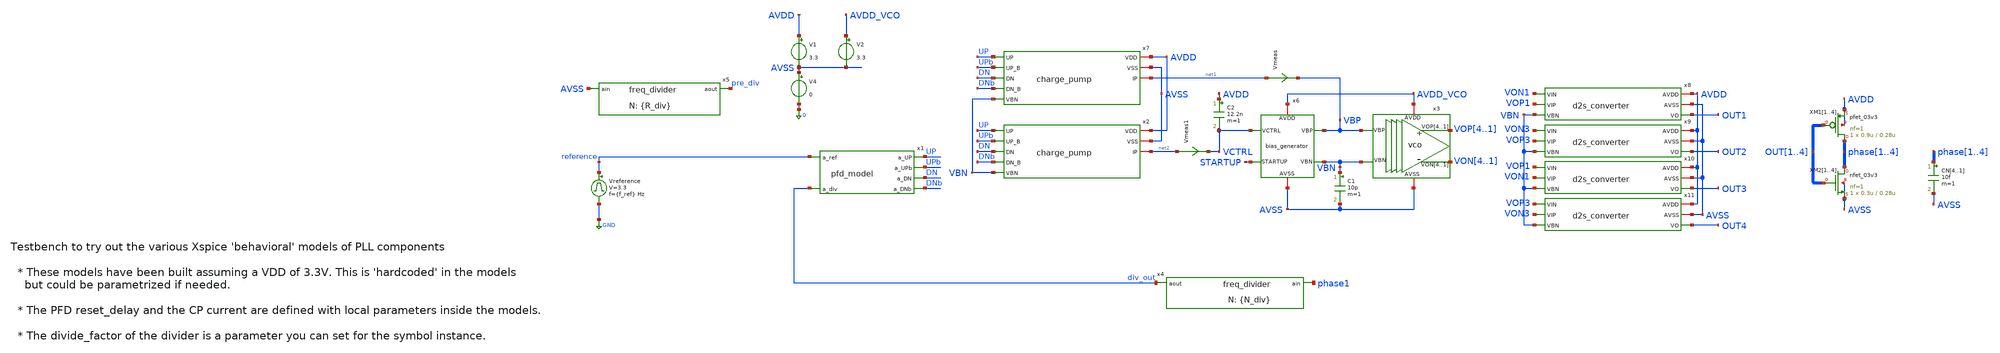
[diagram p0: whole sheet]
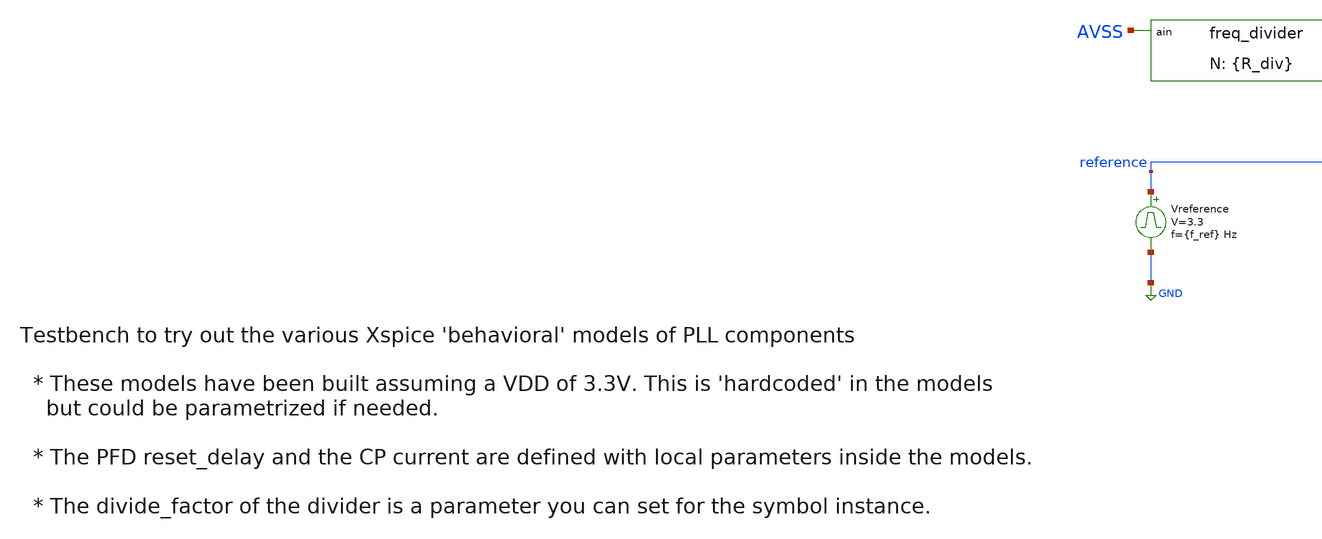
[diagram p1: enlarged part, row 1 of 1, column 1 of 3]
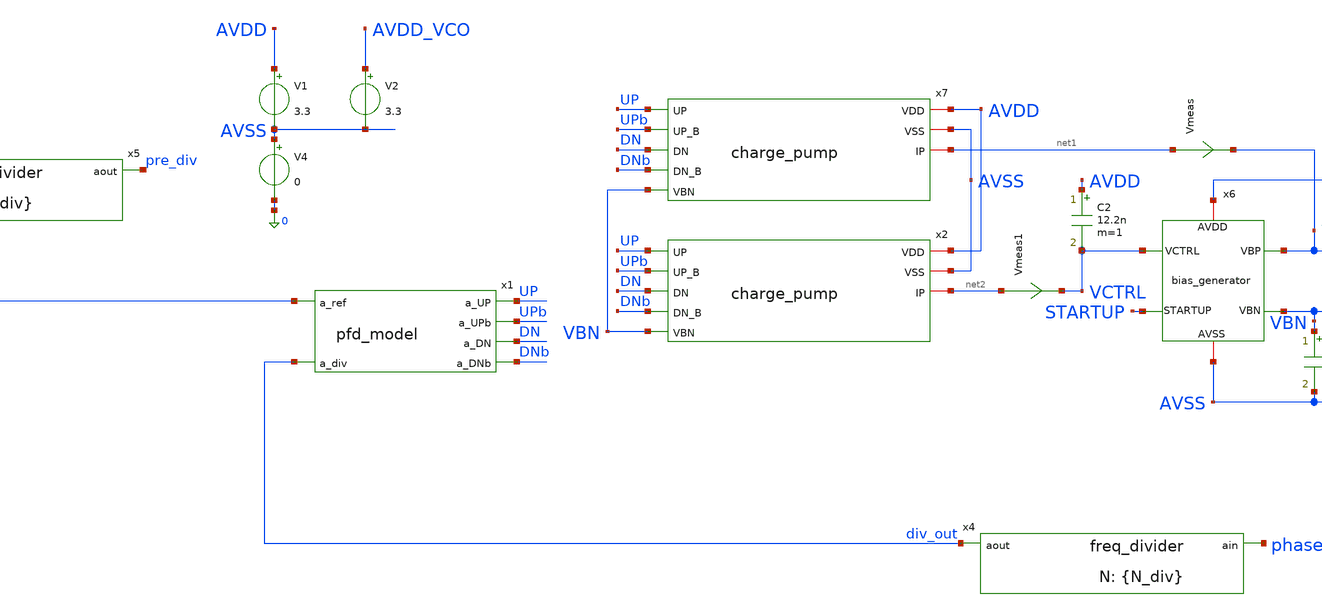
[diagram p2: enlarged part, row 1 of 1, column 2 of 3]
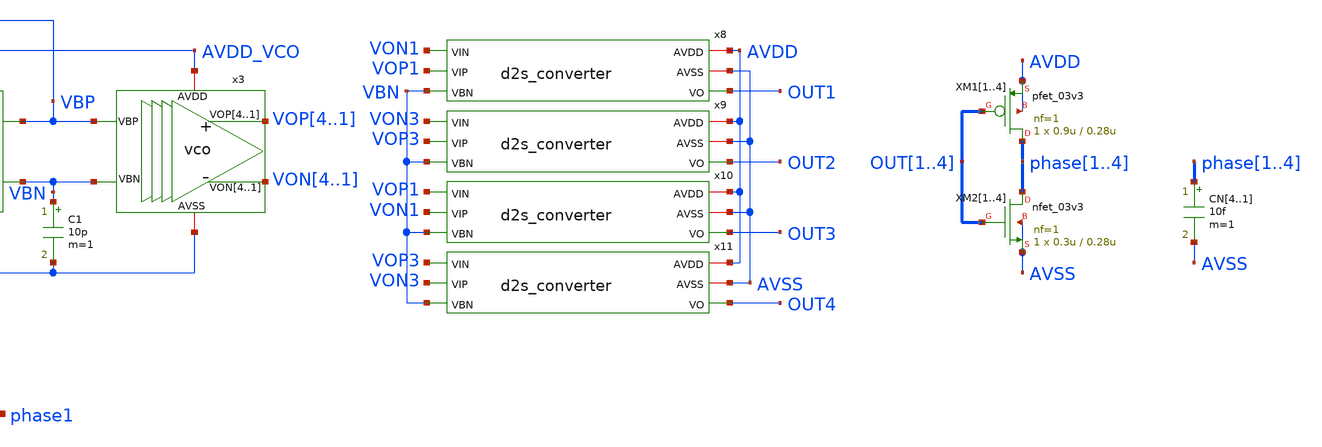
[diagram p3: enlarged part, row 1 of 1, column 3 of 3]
** sch_path: designs/libs/tb_pll/tb_PLL_CP_VCO_model_v2.sch
**.subckt tb_PLL_CP_VCO_model_v2
Vreference reference GND pulse 0 3.3 '0.495/ {f_ref} ' '0.01/{f_ref} ' '0.01/{f_ref} ' '0.49/{f_ref} '
+ '1/{f_ref} '
x1 reference UP UPb DN div_out DNb pfd_model
x4 div_out phase1 freq_divider divide_factor={N_div}
x5 pre_div AVSS freq_divider divide_factor={R_div}
x3 VOP4 VOP3 VOP2 VOP1 VON4 VON3 VON2 VON1 AVDD_VCO AVSS VBP VBN vco
x6 VCTRL AVDD_VCO STARTUP AVSS VBP VBN bias_generator
C1 VBN AVSS 10p m=1
C2 AVDD VCTRL 12.2n m=1
x8 AVDD AVSS VON1 VOP1 VBN OUT1 d2s_converter
XM11 phase1 OUT1 AVDD AVDD pfet_03v3 L=0.28u W=0.9u nf=1 ad='int((nf+1)/2) * W/nf * 0.18u' as='int((nf+2)/2) * W/nf * 0.18u'
+ pd='2*int((nf+1)/2) * (W/nf + 0.18u)' ps='2*int((nf+2)/2) * (W/nf + 0.18u)' nrd='0.18u / W' nrs='0.18u / W'
+ sa=0 sb=0 sd=0 m=1
XM12 phase2 OUT2 AVDD AVDD pfet_03v3 L=0.28u W=0.9u nf=1 ad='int((nf+1)/2) * W/nf * 0.18u' as='int((nf+2)/2) * W/nf * 0.18u'
+ pd='2*int((nf+1)/2) * (W/nf + 0.18u)' ps='2*int((nf+2)/2) * (W/nf + 0.18u)' nrd='0.18u / W' nrs='0.18u / W'
+ sa=0 sb=0 sd=0 m=1
XM13 phase3 OUT3 AVDD AVDD pfet_03v3 L=0.28u W=0.9u nf=1 ad='int((nf+1)/2) * W/nf * 0.18u' as='int((nf+2)/2) * W/nf * 0.18u'
+ pd='2*int((nf+1)/2) * (W/nf + 0.18u)' ps='2*int((nf+2)/2) * (W/nf + 0.18u)' nrd='0.18u / W' nrs='0.18u / W'
+ sa=0 sb=0 sd=0 m=1
XM14 phase4 OUT4 AVDD AVDD pfet_03v3 L=0.28u W=0.9u nf=1 ad='int((nf+1)/2) * W/nf * 0.18u' as='int((nf+2)/2) * W/nf * 0.18u'
+ pd='2*int((nf+1)/2) * (W/nf + 0.18u)' ps='2*int((nf+2)/2) * (W/nf + 0.18u)' nrd='0.18u / W' nrs='0.18u / W'
+ sa=0 sb=0 sd=0 m=1
XM21 phase1 OUT1 AVSS AVSS nfet_03v3 L=0.28u W=0.3u nf=1 ad='int((nf+1)/2) * W/nf * 0.18u' as='int((nf+2)/2) * W/nf * 0.18u'
+ pd='2*int((nf+1)/2) * (W/nf + 0.18u)' ps='2*int((nf+2)/2) * (W/nf + 0.18u)' nrd='0.18u / W' nrs='0.18u / W'
+ sa=0 sb=0 sd=0 m=1
XM22 phase2 OUT2 AVSS AVSS nfet_03v3 L=0.28u W=0.3u nf=1 ad='int((nf+1)/2) * W/nf * 0.18u' as='int((nf+2)/2) * W/nf * 0.18u'
+ pd='2*int((nf+1)/2) * (W/nf + 0.18u)' ps='2*int((nf+2)/2) * (W/nf + 0.18u)' nrd='0.18u / W' nrs='0.18u / W'
+ sa=0 sb=0 sd=0 m=1
XM23 phase3 OUT3 AVSS AVSS nfet_03v3 L=0.28u W=0.3u nf=1 ad='int((nf+1)/2) * W/nf * 0.18u' as='int((nf+2)/2) * W/nf * 0.18u'
+ pd='2*int((nf+1)/2) * (W/nf + 0.18u)' ps='2*int((nf+2)/2) * (W/nf + 0.18u)' nrd='0.18u / W' nrs='0.18u / W'
+ sa=0 sb=0 sd=0 m=1
XM24 phase4 OUT4 AVSS AVSS nfet_03v3 L=0.28u W=0.3u nf=1 ad='int((nf+1)/2) * W/nf * 0.18u' as='int((nf+2)/2) * W/nf * 0.18u'
+ pd='2*int((nf+1)/2) * (W/nf + 0.18u)' ps='2*int((nf+2)/2) * (W/nf + 0.18u)' nrd='0.18u / W' nrs='0.18u / W'
+ sa=0 sb=0 sd=0 m=1
x9 AVDD AVSS VON3 VOP3 VBN OUT2 d2s_converter
x10 AVDD AVSS VOP1 VON1 VBN OUT3 d2s_converter
x11 AVDD AVSS VOP3 VON3 VBN OUT4 d2s_converter
V1 AVDD AVSS 3.3
V4 AVSS 0 0
V2 AVDD_VCO AVSS 3.3
CN4 phase1 AVSS 10f m=1
CN3 phase2 AVSS 10f m=1
CN2 phase3 AVSS 10f m=1
CN1 phase4 AVSS 10f m=1
Vmeas net1 VBP 0
.save i(vmeas)
Vmeas1 net2 VCTRL 0
.save i(vmeas1)
x2 AVDD AVSS UP UPb DN DNb VBN net2 charge_pump
x7 AVDD AVSS UP UPb DN DNb VBN net1 charge_pump
**** begin user architecture code


.param f_ref=10MEG R_div=2 N_div=20
.ic v(vop1)=3.3 v(von1)=0 v(startup)=0 v(VCTRL)=1 v(vbp)=1

.param d1=0 d2=3.3 d3=3.3 d4=0
.param d1b=3.3 d2b=0 d3b=0 d4b=3.3

VS1 S1 0 d1
VS2 S2 0 d2
VS3 S3 0 d3
VS4 S4 0 d4

VS1b S1b 0 d1b
VS2b S2b 0 d2b
VS3b S3b 0 d3b
VS4b S4b 0 d4b

.control

save all

OP
show all

tran 1n 10u

remzerovec

write tb_PLL_CP_VCO_model_v2.raw
.endc



.include $::180MCU_MODELS/design.ngspice
.lib $::180MCU_MODELS/sm141064.ngspice typical
*.lib $::180MCU_MODELS/sm141064.ngspice SS
*.lib $::180MCU_MODELS/sm141064.ngspice FF
*.lib $::180MCU_MODELS/sm141064.ngspice SF
*.lib $::180MCU_MODELS/sm141064.ngspice FS

**** end user architecture code
**.ends

* expanding   symbol:  libs/model_pll/pfd_model.sym # of pins=6
** sym_path: designs/libs/model_pll/pfd_model.sym
** sch_path: designs/libs/model_pll/pfd_model.sch
.subckt pfd_model a_ref a_UP a_UPb a_DN a_div a_DNb
*.ipin a_ref
*.ipin a_div
*.opin a_UP
*.opin a_UPb
*.opin a_DN
*.opin a_DNb
* noconn a_ref
* noconn a_div
* noconn a_UP
* noconn a_UPb
* noconn a_DN
* noconn a_DNb
**** begin user architecture code


* PFD Model using digital Xspice components

* pfd_delay local parameter sets the duration of the overlap (dead-band elimination)
* Reduced from 10ns to 200ps to prevent massive Vctrl ripple
*.param pfd_delay = 200p
.param pfd_delay = 1.5n

** Digital 1 and 0 to drive Flip-Flops
aone 0 d_d1 d_inv
azero d_d1 d_d0 d_inv
.model d_inv d_inverter()

** Flip Flops
ad1 d_d1 d_R d_d0 d_rset d_U d_U_ flop1
ad2 d_d1 d_V d_d0 d_rset d_D d_D_ flop1
.model flop1 d_dff(clk_delay = 1.0e-10 set_delay = 1.0e-10  reset_delay = {pfd_delay} ic = 2 rise_delay
+ = 1.0e-10  fall_delay = 1e-10)

* AND Gate
aa1 [d_U d_D] d_rset and1
.model and1 d_and(rise_delay = 1e-10 fall_delay = 1e-10   input_load = 0.5e-12)

* WINDOW FIX: Widened thresholds to catch fast analog edges safely
aADC [ a_ref a_div ] [ d_R d_V ] adc_buff
.model adc_buff adc_bridge(in_low = 1.2 in_high = 2.1 rise_delay = 10p fall_delay = 10p)

* DAC FIX: Explicitly defined analog rise/fall times to prevent solver crashes
aDAC [ d_U d_U_ d_D d_D_ d_rset d_R d_V d_d1 d_d0 ] [ a_UP a_UPb a_DN a_DNb a_rset a_R a_V a_d1
+ a_d0] dac_buff
.model dac_buff dac_bridge(out_low = 0 out_high = 3.3 t_rise = 500p t_fall = 500p)


**** end user architecture code
.ends


* expanding   symbol:  libs/model_pll/freq_divider.sym # of pins=2
** sym_path: libs/model_pll/freq_divider.sym
** sch_path: libs/model_pll/freq_divider.sch
.subckt freq_divider aout ain  divide_factor=20
*.ipin ain
*.opin aout
* noconn ain
* noconn aout
**** begin user architecture code


* Behavioral Frequency Divider with robust Mixed-Signal Bridges

* Top-level parameter (Defaults to 10 if not passed by symbol)
.param divide_factor = 10

* MATH FIX: Guarantees at least 1 high cycle, targets 50% duty cycle
.param high_cycles = {max(1, floor(divide_factor/2))}

* Xspice digital frequency divider
adiv din dout divider
.model divider d_fdiv(div_factor = {divide_factor}  high_cycles = {high_cycles}  i_count = 0  rise_delay
+ = 10p fall_delay = 10p )

* WINDOW FIX: Widened analog-to-digital thresholds to catch fast sine waves
aADC [ ain ] [ din ] adc_buff
.model adc_buff adc_bridge(in_low = 1.2 in_high = 2.1 rise_delay = 10p fall_delay = 10p)

* Digital-to-analog bridge
aDAC [ dout ] [ aout ] dac_buff
.model dac_buff dac_bridge(out_low = 0 out_high = 3.3 t_rise = 10p t_fall = 10p)


**** end user architecture code
.ends


* expanding   symbol:  libs/core_analog/vco/vco.sym # of pins=6
** sym_path: designs/libs/core_analog/vco/vco.sym
** sch_path: designs/libs/core_analog/vco/vco.sch
.subckt vco VOP4 VOP3 VOP2 VOP1 VON4 VON3 VON2 VON1 AVDD AVSS VBP VBN
*.opin VOP1,VOP2,VOP3,VOP4
*.opin VON1,VON2,VON3,VON4
*.ipin VBP
*.ipin VBN
*.iopin AVDD
*.iopin AVSS
x1 VOP1 AVDD VOP4 VON4 VON1 AVSS VBP VBN delay_stage
x2 VOP2 AVDD VON1 VOP1 VON2 AVSS VBP VBN delay_stage
x3 VOP3 AVDD VON2 VOP2 VON3 AVSS VBP VBN delay_stage
x4 VOP4 AVDD VON3 VOP3 VON4 AVSS VBP VBN delay_stage
.ends


* expanding   symbol:  libs/core_analog/bias_generator/bias_generator.sym # of pins=6
** sym_path: designs/libs/core_analog/bias_generator/bias_generator.sym
** sch_path: designs/libs/core_analog/bias_generator/bias_generator.sch
.subckt bias_generator VCTRL AVDD STARTUP AVSS VBP VBN
*.ipin VCTRL
*.ipin STARTUP
*.iopin AVDD
*.iopin AVSS
*.opin VBP
*.opin VBN
x1 VBN AVDD net2 VCTRL AVSS net1 ota_5t
Vmeas net6 net3 0
.save i(vmeas)
Vmeas1 net7 net5 0
.save i(vmeas1)
Vmeas2 net8 net4 0
.save i(vmeas2)
XM1 net1 net1 AVDD AVDD pfet_03v3 L=0.5u W=16.8u nf=1 ad='int((nf+1)/2) * W/nf * 0.18u' as='int((nf+2)/2) * W/nf * 0.18u'
+ pd='2*int((nf+1)/2) * (W/nf + 0.18u)' ps='2*int((nf+2)/2) * (W/nf + 0.18u)' nrd='0.18u / W' nrs='0.18u / W'
+ sa=0 sb=0 sd=0 m=16
XM8 net2 AVDD net7 AVSS nfet_03v3 L=0.5u W=2.08u nf=1 ad='int((nf+1)/2) * W/nf * 0.18u' as='int((nf+2)/2) * W/nf * 0.18u'
+ pd='2*int((nf+1)/2) * (W/nf + 0.18u)' ps='2*int((nf+2)/2) * (W/nf + 0.18u)' nrd='0.18u / W' nrs='0.18u / W'
+ sa=0 sb=0 sd=0 m=8
XM9 VBP AVDD net8 AVSS nfet_03v3 L=0.5u W=2.08u nf=1 ad='int((nf+1)/2) * W/nf * 0.18u' as='int((nf+2)/2) * W/nf * 0.18u'
+ pd='2*int((nf+1)/2) * (W/nf + 0.18u)' ps='2*int((nf+2)/2) * (W/nf + 0.18u)' nrd='0.18u / W' nrs='0.18u / W'
+ sa=0 sb=0 sd=0 m=56
XM11 net1 AVDD net6 AVSS nfet_03v3 L=0.5u W=2.08u nf=1 ad='int((nf+1)/2) * W/nf * 0.18u' as='int((nf+2)/2) * W/nf * 0.18u'
+ pd='2*int((nf+1)/2) * (W/nf + 0.18u)' ps='2*int((nf+2)/2) * (W/nf + 0.18u)' nrd='0.18u / W' nrs='0.18u / W'
+ sa=0 sb=0 sd=0 m=8
XM12 net4 VBN AVSS AVSS nfet_03v3 L=0.5u W=11.25u nf=1 ad='int((nf+1)/2) * W/nf * 0.18u' as='int((nf+2)/2) * W/nf * 0.18u'
+ pd='2*int((nf+1)/2) * (W/nf + 0.18u)' ps='2*int((nf+2)/2) * (W/nf + 0.18u)' nrd='0.18u / W' nrs='0.18u / W'
+ sa=0 sb=0 sd=0 m=56
XM3 net5 VBN AVSS AVSS nfet_03v3 L=0.5u W=11.25u nf=1 ad='int((nf+1)/2) * W/nf * 0.18u' as='int((nf+2)/2) * W/nf * 0.18u'
+ pd='2*int((nf+1)/2) * (W/nf + 0.18u)' ps='2*int((nf+2)/2) * (W/nf + 0.18u)' nrd='0.18u / W' nrs='0.18u / W'
+ sa=0 sb=0 sd=0 m=8
XM4 net3 VBN AVSS AVSS nfet_03v3 L=0.5u W=11.25u nf=1 ad='int((nf+1)/2) * W/nf * 0.18u' as='int((nf+2)/2) * W/nf * 0.18u'
+ pd='2*int((nf+1)/2) * (W/nf + 0.18u)' ps='2*int((nf+2)/2) * (W/nf + 0.18u)' nrd='0.18u / W' nrs='0.18u / W'
+ sa=0 sb=0 sd=0 m=8
XM10 net3 STARTUP AVSS AVSS nfet_03v3 L=0.5u W=11.25u nf=1 ad='int((nf+1)/2) * W/nf * 0.18u' as='int((nf+2)/2) * W/nf * 0.18u'
+ pd='2*int((nf+1)/2) * (W/nf + 0.18u)' ps='2*int((nf+2)/2) * (W/nf + 0.18u)' nrd='0.18u / W' nrs='0.18u / W'
+ sa=0 sb=0 sd=0 m=8
XM2 net2 VCTRL AVDD AVDD pfet_03v3 L=1.5u W=1.1u nf=1 ad='int((nf+1)/2) * W/nf * 0.18u' as='int((nf+2)/2) * W/nf * 0.18u'
+ pd='2*int((nf+1)/2) * (W/nf + 0.18u)' ps='2*int((nf+2)/2) * (W/nf + 0.18u)' nrd='0.18u / W' nrs='0.18u / W'
+ sa=0 sb=0 sd=0 m=8
XM5 net2 net2 AVDD AVDD pfet_03v3 L=1.5u W=1.1u nf=1 ad='int((nf+1)/2) * W/nf * 0.18u' as='int((nf+2)/2) * W/nf * 0.18u'
+ pd='2*int((nf+1)/2) * (W/nf + 0.18u)' ps='2*int((nf+2)/2) * (W/nf + 0.18u)' nrd='0.18u / W' nrs='0.18u / W'
+ sa=0 sb=0 sd=0 m=8
XM6 VBP VBP AVDD AVDD pfet_03v3 L=1.5u W=1.1u nf=1 ad='int((nf+1)/2) * W/nf * 0.18u' as='int((nf+2)/2) * W/nf * 0.18u'
+ pd='2*int((nf+1)/2) * (W/nf + 0.18u)' ps='2*int((nf+2)/2) * (W/nf + 0.18u)' nrd='0.18u / W' nrs='0.18u / W'
+ sa=0 sb=0 sd=0 m=56
XM7 VBP VBP AVDD AVDD pfet_03v3 L=1.5u W=1.1u nf=1 ad='int((nf+1)/2) * W/nf * 0.18u' as='int((nf+2)/2) * W/nf * 0.18u'
+ pd='2*int((nf+1)/2) * (W/nf + 0.18u)' ps='2*int((nf+2)/2) * (W/nf + 0.18u)' nrd='0.18u / W' nrs='0.18u / W'
+ sa=0 sb=0 sd=0 m=56
.ends


* expanding   symbol:  libs/core_analog/d2s_converter/d2s_converter.sym # of pins=6
** sym_path: designs/libs/core_analog/d2s_converter/d2s_converter.sym
** sch_path: designs/libs/core_analog/d2s_converter/d2s_converter.sch
.subckt d2s_converter AVDD AVSS VIN VIP VBN VO
*.iopin AVDD
*.iopin AVSS
*.ipin VIN
*.ipin VIP
*.opin VO
*.ipin VBN
XM2 VOPB VIN i1 AVSS nfet_03v3 L=0.3u W=1.9u nf=1 ad='int((nf+1)/2) * W/nf * 0.18u' as='int((nf+2)/2) * W/nf * 0.18u'
+ pd='2*int((nf+1)/2) * (W/nf + 0.18u)' ps='2*int((nf+2)/2) * (W/nf + 0.18u)' nrd='0.18u / W' nrs='0.18u / W'
+ sa=0 sb=0 sd=0 m=4
XM4 VOPB VOPB AVDD AVDD pfet_03v3 L=0.3u W=1.4u nf=1 ad='int((nf+1)/2) * W/nf * 0.18u' as='int((nf+2)/2) * W/nf * 0.18u'
+ pd='2*int((nf+1)/2) * (W/nf + 0.18u)' ps='2*int((nf+2)/2) * (W/nf + 0.18u)' nrd='0.18u / W' nrs='0.18u / W'
+ sa=0 sb=0 sd=0 m=4
XM11 VOB VOB AVSS AVSS nfet_03v3 L=0.3u W=1.5u nf=1 ad='int((nf+1)/2) * W/nf * 0.18u' as='int((nf+2)/2) * W/nf * 0.18u'
+ pd='2*int((nf+1)/2) * (W/nf + 0.18u)' ps='2*int((nf+2)/2) * (W/nf + 0.18u)' nrd='0.18u / W' nrs='0.18u / W'
+ sa=0 sb=0 sd=0 m=4
XM13 VOB VOP AVDD AVDD pfet_03v3 L=0.3u W=2u nf=1 ad='int((nf+1)/2) * W/nf * 0.18u' as='int((nf+2)/2) * W/nf * 0.18u'
+ pd='2*int((nf+1)/2) * (W/nf + 0.18u)' ps='2*int((nf+2)/2) * (W/nf + 0.18u)' nrd='0.18u / W' nrs='0.18u / W'
+ sa=0 sb=0 sd=0 m=4
XM3 VOP VIP i1 AVSS nfet_03v3 L=0.3u W=1.9u nf=1 ad='int((nf+1)/2) * W/nf * 0.18u' as='int((nf+2)/2) * W/nf * 0.18u'
+ pd='2*int((nf+1)/2) * (W/nf + 0.18u)' ps='2*int((nf+2)/2) * (W/nf + 0.18u)' nrd='0.18u / W' nrs='0.18u / W'
+ sa=0 sb=0 sd=0 m=4
XM5 VOP VOPB AVDD AVDD pfet_03v3 L=0.3u W=1.4u nf=1 ad='int((nf+1)/2) * W/nf * 0.18u' as='int((nf+2)/2) * W/nf * 0.18u'
+ pd='2*int((nf+1)/2) * (W/nf + 0.18u)' ps='2*int((nf+2)/2) * (W/nf + 0.18u)' nrd='0.18u / W' nrs='0.18u / W'
+ sa=0 sb=0 sd=0 m=4
XM7 VONB VIP i2 AVSS nfet_03v3 L=0.3u W=1.9u nf=1 ad='int((nf+1)/2) * W/nf * 0.18u' as='int((nf+2)/2) * W/nf * 0.18u'
+ pd='2*int((nf+1)/2) * (W/nf + 0.18u)' ps='2*int((nf+2)/2) * (W/nf + 0.18u)' nrd='0.18u / W' nrs='0.18u / W'
+ sa=0 sb=0 sd=0 m=4
XM8 VONB VONB AVDD AVDD pfet_03v3 L=0.3u W=1.4u nf=1 ad='int((nf+1)/2) * W/nf * 0.18u' as='int((nf+2)/2) * W/nf * 0.18u'
+ pd='2*int((nf+1)/2) * (W/nf + 0.18u)' ps='2*int((nf+2)/2) * (W/nf + 0.18u)' nrd='0.18u / W' nrs='0.18u / W'
+ sa=0 sb=0 sd=0 m=4
XM9 VON VIN i2 AVSS nfet_03v3 L=0.3u W=1.9u nf=1 ad='int((nf+1)/2) * W/nf * 0.18u' as='int((nf+2)/2) * W/nf * 0.18u'
+ pd='2*int((nf+1)/2) * (W/nf + 0.18u)' ps='2*int((nf+2)/2) * (W/nf + 0.18u)' nrd='0.18u / W' nrs='0.18u / W'
+ sa=0 sb=0 sd=0 m=4
XM10 VON VONB AVDD AVDD pfet_03v3 L=0.3u W=1.4u nf=1 ad='int((nf+1)/2) * W/nf * 0.18u' as='int((nf+2)/2) * W/nf * 0.18u'
+ pd='2*int((nf+1)/2) * (W/nf + 0.18u)' ps='2*int((nf+2)/2) * (W/nf + 0.18u)' nrd='0.18u / W' nrs='0.18u / W'
+ sa=0 sb=0 sd=0 m=4
XM14 VO VON AVDD AVDD pfet_03v3 L=0.3u W=2u nf=1 ad='int((nf+1)/2) * W/nf * 0.18u' as='int((nf+2)/2) * W/nf * 0.18u'
+ pd='2*int((nf+1)/2) * (W/nf + 0.18u)' ps='2*int((nf+2)/2) * (W/nf + 0.18u)' nrd='0.18u / W' nrs='0.18u / W'
+ sa=0 sb=0 sd=0 m=4
XM12 VO VOB AVSS AVSS nfet_03v3 L=0.3u W=1.5u nf=1 ad='int((nf+1)/2) * W/nf * 0.18u' as='int((nf+2)/2) * W/nf * 0.18u'
+ pd='2*int((nf+1)/2) * (W/nf + 0.18u)' ps='2*int((nf+2)/2) * (W/nf + 0.18u)' nrd='0.18u / W' nrs='0.18u / W'
+ sa=0 sb=0 sd=0 m=4
XM1 i1 VBN AVSS AVSS nfet_03v3 L=0.5u W=11.25u nf=1 ad='int((nf+1)/2) * W/nf * 0.18u' as='int((nf+2)/2) * W/nf * 0.18u'
+ pd='2*int((nf+1)/2) * (W/nf + 0.18u)' ps='2*int((nf+2)/2) * (W/nf + 0.18u)' nrd='0.18u / W' nrs='0.18u / W'
+ sa=0 sb=0 sd=0 m=4
XM6 i2 VBN AVSS AVSS nfet_03v3 L=0.5u W=11.25u nf=1 ad='int((nf+1)/2) * W/nf * 0.18u' as='int((nf+2)/2) * W/nf * 0.18u'
+ pd='2*int((nf+1)/2) * (W/nf + 0.18u)' ps='2*int((nf+2)/2) * (W/nf + 0.18u)' nrd='0.18u / W' nrs='0.18u / W'
+ sa=0 sb=0 sd=0 m=4
.ends


* expanding   symbol:  libs/core_analog/charge_pump/charge_pump.sym # of pins=8
** sym_path: designs/libs/core_analog/charge_pump/charge_pump.sym
** sch_path: designs/libs/core_analog/charge_pump/charge_pump.sch
.subckt charge_pump VDD VSS UP UP_B DN DN_B VBN IP
*.iopin VDD
*.iopin VSS
*.ipin UP
*.ipin UP_B
*.ipin DN
*.ipin DN_B
*.ipin VBN
*.iopin IP
XM1 net1 VBN net7 VSS nfet_03v3 L=0.6u W=17u nf=1 ad='int((nf+1)/2) * W/nf * 0.18u' as='int((nf+2)/2) * W/nf * 0.18u'
+ pd='2*int((nf+1)/2) * (W/nf + 0.18u)' ps='2*int((nf+2)/2) * (W/nf + 0.18u)' nrd='0.18u / W' nrs='0.18u / W'
+ sa=0 sb=0 sd=0 m=1
XM2 net2 VBN net6 VSS nfet_03v3 L=0.6u W=17u nf=1 ad='int((nf+1)/2) * W/nf * 0.18u' as='int((nf+2)/2) * W/nf * 0.18u'
+ pd='2*int((nf+1)/2) * (W/nf + 0.18u)' ps='2*int((nf+2)/2) * (W/nf + 0.18u)' nrd='0.18u / W' nrs='0.18u / W'
+ sa=0 sb=0 sd=0 m=1
XM3 net5 DN net1 VSS nfet_03v3 L=0.3u W=1.5u nf=1 ad='int((nf+1)/2) * W/nf * 0.18u' as='int((nf+2)/2) * W/nf * 0.18u'
+ pd='2*int((nf+1)/2) * (W/nf + 0.18u)' ps='2*int((nf+2)/2) * (W/nf + 0.18u)' nrd='0.18u / W' nrs='0.18u / W'
+ sa=0 sb=0 sd=0 m=1
XM4 net3 DN_B net1 VSS nfet_03v3 L=0.3u W=1.5u nf=1 ad='int((nf+1)/2) * W/nf * 0.18u' as='int((nf+2)/2) * W/nf * 0.18u'
+ pd='2*int((nf+1)/2) * (W/nf + 0.18u)' ps='2*int((nf+2)/2) * (W/nf + 0.18u)' nrd='0.18u / W' nrs='0.18u / W'
+ sa=0 sb=0 sd=0 m=1
XM5 net4 UP_B net2 VSS nfet_03v3 L=0.3u W=1.5u nf=1 ad='int((nf+1)/2) * W/nf * 0.18u' as='int((nf+2)/2) * W/nf * 0.18u'
+ pd='2*int((nf+1)/2) * (W/nf + 0.18u)' ps='2*int((nf+2)/2) * (W/nf + 0.18u)' nrd='0.18u / W' nrs='0.18u / W'
+ sa=0 sb=0 sd=0 m=1
XM6 IP UP net2 VSS nfet_03v3 L=0.3u W=1.5u nf=1 ad='int((nf+1)/2) * W/nf * 0.18u' as='int((nf+2)/2) * W/nf * 0.18u'
+ pd='2*int((nf+1)/2) * (W/nf + 0.18u)' ps='2*int((nf+2)/2) * (W/nf + 0.18u)' nrd='0.18u / W' nrs='0.18u / W'
+ sa=0 sb=0 sd=0 m=1
x1 net5 net5 VDD net5 VDD cp_sym_load
x2 net3 net3 VDD net3 VDD cp_sym_load
x3 net4 net4 VDD net4 VDD cp_sym_load
x4 net5 net5 VDD IP VDD cp_sym_load
Vtail net7 VSS 0
.save i(vtail)
Vtail2 net6 VSS 0
.save i(vtail2)
.ends


* expanding   symbol:  libs/core_analog/delay_stage/delay_stage.sym # of pins=8
** sym_path: designs/libs/core_analog/delay_stage/delay_stage.sym
** sch_path: designs/libs/core_analog/delay_stage/delay_stage.sch
.subckt delay_stage VOP AVDD VIP VIN VON AVSS VBP VBN
*.ipin VIP
*.ipin VIN
*.opin VOP
*.opin VON
*.iopin AVDD
*.iopin AVSS
*.ipin VBP
*.ipin VBN
XM5 VON VIP net1 AVSS nfet_03v3 L=0.5u W=2.08u nf=1 ad='int((nf+1)/2) * W/nf * 0.18u' as='int((nf+2)/2) * W/nf * 0.18u'
+ pd='2*int((nf+1)/2) * (W/nf + 0.18u)' ps='2*int((nf+2)/2) * (W/nf + 0.18u)' nrd='0.18u / W' nrs='0.18u / W'
+ sa=0 sb=0 sd=0 m=8
XM2 VON VON AVDD AVDD pfet_03v3 L=1.5u W=1.1u nf=1 ad='int((nf+1)/2) * W/nf * 0.18u' as='int((nf+2)/2) * W/nf * 0.18u'
+ pd='2*int((nf+1)/2) * (W/nf + 0.18u)' ps='2*int((nf+2)/2) * (W/nf + 0.18u)' nrd='0.18u / W' nrs='0.18u / W'
+ sa=0 sb=0 sd=0 m=8
XM6 VOP VIN net1 AVSS nfet_03v3 L=0.5u W=2.08u nf=1 ad='int((nf+1)/2) * W/nf * 0.18u' as='int((nf+2)/2) * W/nf * 0.18u'
+ pd='2*int((nf+1)/2) * (W/nf + 0.18u)' ps='2*int((nf+2)/2) * (W/nf + 0.18u)' nrd='0.18u / W' nrs='0.18u / W'
+ sa=0 sb=0 sd=0 m=8
XM1 VON VBP AVDD AVDD pfet_03v3 L=1.5u W=1.1u nf=1 ad='int((nf+1)/2) * W/nf * 0.18u' as='int((nf+2)/2) * W/nf * 0.18u'
+ pd='2*int((nf+1)/2) * (W/nf + 0.18u)' ps='2*int((nf+2)/2) * (W/nf + 0.18u)' nrd='0.18u / W' nrs='0.18u / W'
+ sa=0 sb=0 sd=0 m=8
XM3 VOP VBP AVDD AVDD pfet_03v3 L=1.5u W=1.1u nf=1 ad='int((nf+1)/2) * W/nf * 0.18u' as='int((nf+2)/2) * W/nf * 0.18u'
+ pd='2*int((nf+1)/2) * (W/nf + 0.18u)' ps='2*int((nf+2)/2) * (W/nf + 0.18u)' nrd='0.18u / W' nrs='0.18u / W'
+ sa=0 sb=0 sd=0 m=8
XM4 VOP VOP AVDD AVDD pfet_03v3 L=1.5u W=1.1u nf=1 ad='int((nf+1)/2) * W/nf * 0.18u' as='int((nf+2)/2) * W/nf * 0.18u'
+ pd='2*int((nf+1)/2) * (W/nf + 0.18u)' ps='2*int((nf+2)/2) * (W/nf + 0.18u)' nrd='0.18u / W' nrs='0.18u / W'
+ sa=0 sb=0 sd=0 m=8
XM8 net1 VBN AVSS AVSS nfet_03v3 L=0.5u W=11.25u nf=1 ad='int((nf+1)/2) * W/nf * 0.18u' as='int((nf+2)/2) * W/nf * 0.18u'
+ pd='2*int((nf+1)/2) * (W/nf + 0.18u)' ps='2*int((nf+2)/2) * (W/nf + 0.18u)' nrd='0.18u / W' nrs='0.18u / W'
+ sa=0 sb=0 sd=0 m=8
.ends


* expanding   symbol:  libs/core_analog/ota_5t/ota_5t.sym # of pins=6
** sym_path: designs/libs/core_analog/ota_5t/ota_5t.sym
** sch_path: designs/libs/core_analog/ota_5t/ota_5t.sch
.subckt ota_5t VO AVDD VI+ VI- AVSS VB
*.ipin VI+
*.ipin VI-
*.ipin VB
*.iopin AVDD
*.iopin AVSS
*.opin VO
XM1 VO VI- net2 AVDD pfet_03v3 L=0.5u W=6.55u nf=1 ad='int((nf+1)/2) * W/nf * 0.18u' as='int((nf+2)/2) * W/nf * 0.18u'
+ pd='2*int((nf+1)/2) * (W/nf + 0.18u)' ps='2*int((nf+2)/2) * (W/nf + 0.18u)' nrd='0.18u / W' nrs='0.18u / W'
+ sa=0 sb=0 sd=0 m=8
XM4 VO net1 AVSS AVSS nfet_03v3 L=0.5u W=4.8u nf=1 ad='int((nf+1)/2) * W/nf * 0.18u' as='int((nf+2)/2) * W/nf * 0.18u'
+ pd='2*int((nf+1)/2) * (W/nf + 0.18u)' ps='2*int((nf+2)/2) * (W/nf + 0.18u)' nrd='0.18u / W' nrs='0.18u / W'
+ sa=0 sb=0 sd=0 m=4
XM3 net2 VB net3 AVDD pfet_03v3 L=0.5u W=16.8u nf=1 ad='int((nf+1)/2) * W/nf * 0.18u' as='int((nf+2)/2) * W/nf * 0.18u'
+ pd='2*int((nf+1)/2) * (W/nf + 0.18u)' ps='2*int((nf+2)/2) * (W/nf + 0.18u)' nrd='0.18u / W' nrs='0.18u / W'
+ sa=0 sb=0 sd=0 m=16
XM2 net1 VI+ net2 AVDD pfet_03v3 L=0.5u W=6.55u nf=1 ad='int((nf+1)/2) * W/nf * 0.18u' as='int((nf+2)/2) * W/nf * 0.18u'
+ pd='2*int((nf+1)/2) * (W/nf + 0.18u)' ps='2*int((nf+2)/2) * (W/nf + 0.18u)' nrd='0.18u / W' nrs='0.18u / W'
+ sa=0 sb=0 sd=0 m=8
XM5 net1 net1 AVSS AVSS nfet_03v3 L=0.5u W=4.8u nf=1 ad='int((nf+1)/2) * W/nf * 0.18u' as='int((nf+2)/2) * W/nf * 0.18u'
+ pd='2*int((nf+1)/2) * (W/nf + 0.18u)' ps='2*int((nf+2)/2) * (W/nf + 0.18u)' nrd='0.18u / W' nrs='0.18u / W'
+ sa=0 sb=0 sd=0 m=4
Vmeas AVDD net3 0
.save i(vmeas)
.ends


* expanding   symbol:
*+  /foss/designs/synchronos-chipathon-2026/designs/libs/core_analog/cp_sym_load/cp_sym_load.sym # of pins=5
** sym_path: designs/libs/core_analog/cp_sym_load/cp_sym_load.sym
** sch_path: designs/libs/core_analog/cp_sym_load/cp_sym_load.sch
.subckt cp_sym_load G1 G2 S D VDD
*.ipin G1
*.ipin G2
*.iopin S
*.iopin D
*.iopin VDD
XM1 D G1 S VDD pfet_03v3 L=1.5u W=1.1u nf=1 ad='int((nf+1)/2) * W/nf * 0.18u' as='int((nf+2)/2) * W/nf * 0.18u'
+ pd='2*int((nf+1)/2) * (W/nf + 0.18u)' ps='2*int((nf+2)/2) * (W/nf + 0.18u)' nrd='0.18u / W' nrs='0.18u / W'
+ sa=0 sb=0 sd=0 m=1
XM2 D G2 S VDD pfet_03v3 L=1.5u W=1.1u nf=1 ad='int((nf+1)/2) * W/nf * 0.18u' as='int((nf+2)/2) * W/nf * 0.18u'
+ pd='2*int((nf+1)/2) * (W/nf + 0.18u)' ps='2*int((nf+2)/2) * (W/nf + 0.18u)' nrd='0.18u / W' nrs='0.18u / W'
+ sa=0 sb=0 sd=0 m=1
.ends

.GLOBAL GND
.end
